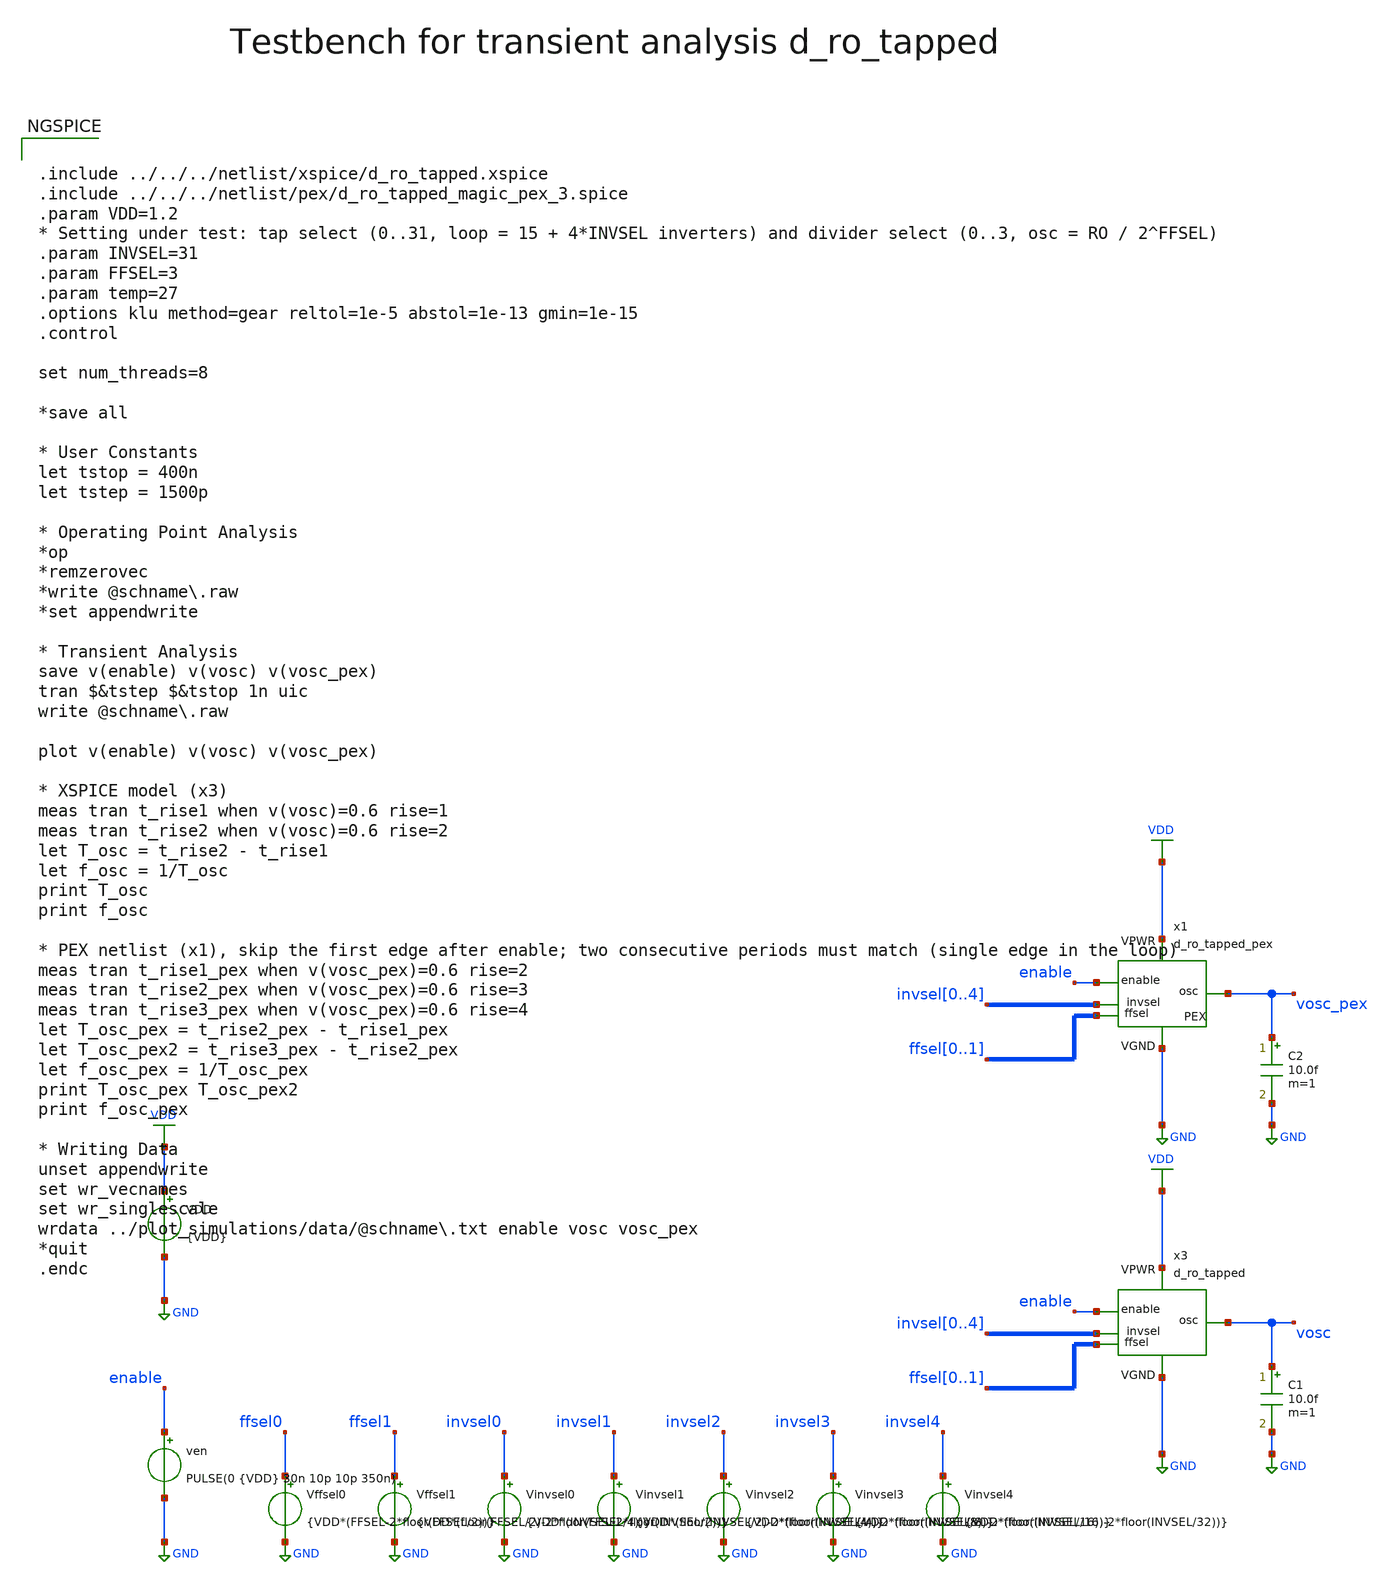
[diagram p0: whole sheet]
** sch_path: macros/heichips26_digital_project/macros/d_ro_tapped/testbenches/xschem/d_ro_tapped_tb_tran.sch
**.subckt d_ro_tapped_tb_tran
VDD VDD GND {VDD}
ven enable GND PULSE(0 {VDD} 30n 10p 10p 350n)
x1 VDD GND enable vosc_pex ffsel0 ffsel1 invsel0 invsel1 invsel2 invsel3 invsel4 d_ro_tapped_pex
C1 vosc GND 10.0f m=1
x3 VDD GND enable vosc ffsel0 ffsel1 invsel0 invsel1 invsel2 invsel3 invsel4 d_ro_tapped
Vffsel0 ffsel0 GND {VDD*(FFSEL-2*floor(FFSEL/2))}
Vffsel1 ffsel1 GND {VDD*(floor(FFSEL/2)-2*floor(FFSEL/4))}
Vinvsel0 invsel0 GND {VDD*(INVSEL-2*floor(INVSEL/2))}
Vinvsel1 invsel1 GND {VDD*(floor(INVSEL/2)-2*floor(INVSEL/4))}
Vinvsel2 invsel2 GND {VDD*(floor(INVSEL/4)-2*floor(INVSEL/8))}
Vinvsel3 invsel3 GND {VDD*(floor(INVSEL/8)-2*floor(INVSEL/16))}
Vinvsel4 invsel4 GND {VDD*(floor(INVSEL/16)-2*floor(INVSEL/32))}
C2 vosc_pex GND 10.0f m=1
**** begin user architecture code


.include ../../../netlist/xspice/d_ro_tapped.xspice
.include ../../../netlist/pex/d_ro_tapped_magic_pex_3.spice
.param VDD=1.2
* Setting under test: tap select (0..31, loop = 15 + 4*INVSEL inverters) and divider select (0..3,
*+ osc = RO / 2^FFSEL)
.param INVSEL=31
.param FFSEL=3
.param temp=27
.options klu method=gear reltol=1e-5 abstol=1e-13 gmin=1e-15
.control

set num_threads=8

*save all

* User Constants
let tstop = 400n
let tstep = 1500p

* Operating Point Analysis
*op
*remzerovec
*write @schname\.raw
*set appendwrite

* Transient Analysis
save v(enable) v(vosc) v(vosc_pex)
tran $&tstep $&tstop 1n uic
write @schname\.raw

plot v(enable) v(vosc) v(vosc_pex)

* XSPICE model (x3)
meas tran t_rise1 when v(vosc)=0.6 rise=1
meas tran t_rise2 when v(vosc)=0.6 rise=2
let T_osc = t_rise2 - t_rise1
let f_osc = 1/T_osc
print T_osc
print f_osc

* PEX netlist (x1), skip the first edge after enable; two consecutive periods must match (single
*+ edge in the loop)
meas tran t_rise1_pex when v(vosc_pex)=0.6 rise=2
meas tran t_rise2_pex when v(vosc_pex)=0.6 rise=3
meas tran t_rise3_pex when v(vosc_pex)=0.6 rise=4
let T_osc_pex = t_rise2_pex - t_rise1_pex
let T_osc_pex2 = t_rise3_pex - t_rise2_pex
let f_osc_pex = 1/T_osc_pex
print T_osc_pex T_osc_pex2
print f_osc_pex

* Writing Data
unset appendwrite
set wr_vecnames
set wr_singlescale
wrdata ../plot_simulations/data/@schname\.txt enable vosc vosc_pex
*quit
.endc


.lib cornerMOSlv.lib mos_tt
.lib cornerMOShv.lib mos_tt
.lib cornerRES.lib res_typ
.lib cornerDIO.lib dio_tt

**** end user architecture code
**.ends
.GLOBAL GND
.GLOBAL VDD
.end
